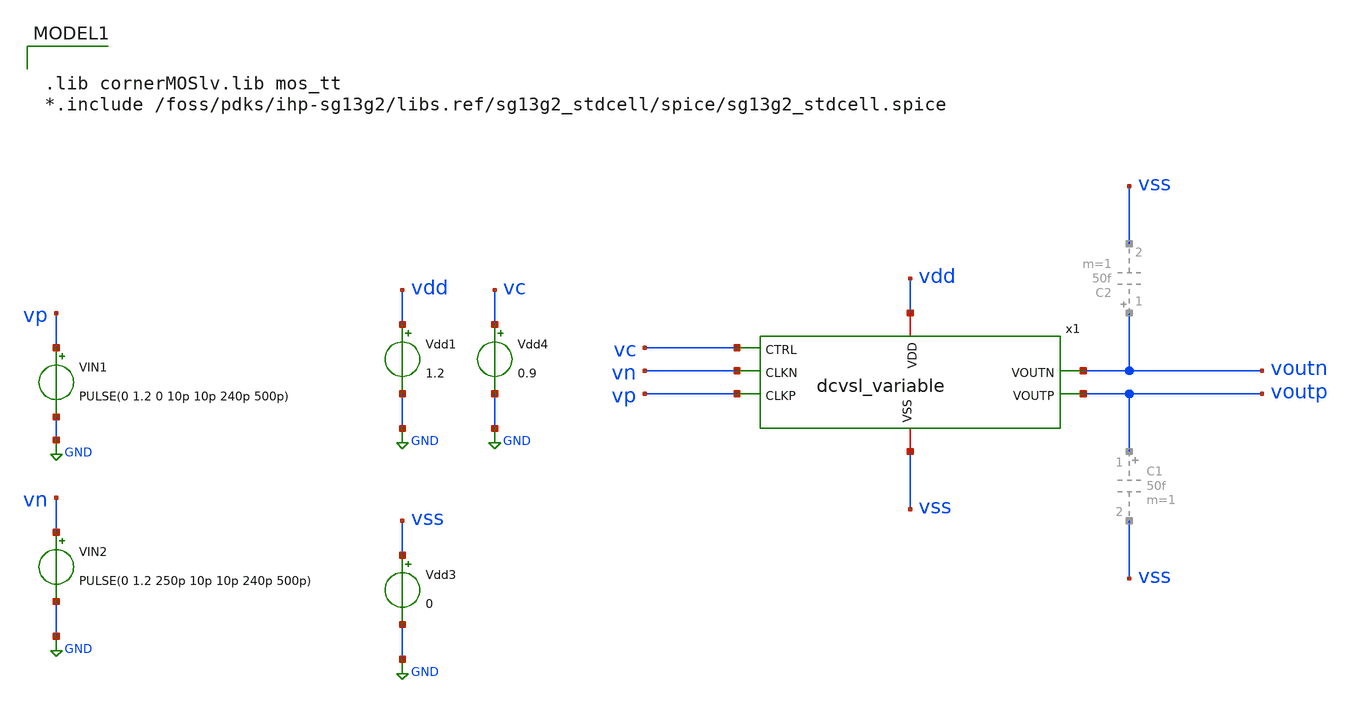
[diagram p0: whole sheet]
** sch_path: verification/testbenches/tb_delay_variable.sch
**.subckt tb_delay_variable
x1 vdd voutn voutp vc vn vp vss dcvsl_variable
Vdd1 vdd GND 1.2
VIN1 vp GND PULSE(0 1.2 0 10p 10p 240p 500p)
VIN2 vn GND PULSE(0 1.2 250p 10p 10p 240p 500p)
Vdd4 vc GND 0.9
Vdd3 vss GND 0
**** begin user architecture code

.lib cornerMOSlv.lib mos_tt
*.include /foss/pdks/ihp-sg13g2/libs.ref/sg13g2_stdcell/spice/sg13g2_stdcell.spice




.save v(vp) v(vn) v(voutn) v(voup)

.tran 5p 3n
.save all

.control
run
set color0=white
write tran_logic.raw



meas tran SKEW0_90 TRIG v(vp) VAL=0.6 RISE=3 TARG v(voutp) VAL=0.6 RISE=2
meas tran SKEW90_180 TRIG v(voutp) VAL=0.6 RISE=2 TARG v(vn) VAL=0.6 RISE=3
meas tran SKEW180_270 TRIG v(vn) VAL=0.6 RISE=3 TARG v(voutn) VAL=0.6 RISE=3
meas tran SKEW270_0 TRIG v(voutn) VAL=0.6 RISE=3 TARG v(vp) VAL=0.6 RISE=4

*meas tran T90 TRIG v(voutp) VAL=0.6 RISE=3 TARG v(v90) VAL=0.6 RISE=4
*meas tran T180 TRIG v(vn) VAL=0.6 RISE=3 TARG v(v180) VAL=0.6 RISE=4
*meas tran T270 TRIG v(voutn) VAL=0.6 RISE=3 TARG v(v270) VAL=0.6 RISE=4
*meas tran T0 TRIG v(vp) VAL=0.6 RISE=3 TARG v(v0) VAL=0.6 RISE=4

let phase0_90 = (SKEW0_90 / 500p) * 360
let phase90_180 = (SKEW90_180 / 500p) * 360
let phase180_270 = (SKEW180_270 / 500p) * 360
let phase270_0 = (SKEW270_0 / 500p) * 360


meas tran PW0 TRIG v(vp) VAL=0.6 RISE=3 TARG v(vp) VAL=0.6 FALL=3
meas tran PW90 TRIG v(voutp) VAL=0.6 RISE=3 TARG v(voutp) VAL=0.6 FALL=4
meas tran PW180 TRIG v(vn) VAL=0.6 RISE=3 TARG v(vn) VAL=0.6 FALL=3
meas tran PW270 TRIG v(voutn) VAL=0.6 RISE=3 TARG v(voutn) VAL=0.6 FALL=4

print SKEW0_90 SKEW90_180 SKEW180_270 SKEW270_0 phase0_90 phase90_180 phase180_270 phase270_0 PW0
+ PW90 PW180 PW270

.endc


**** end user architecture code
**.ends
.GLOBAL GND
.end
